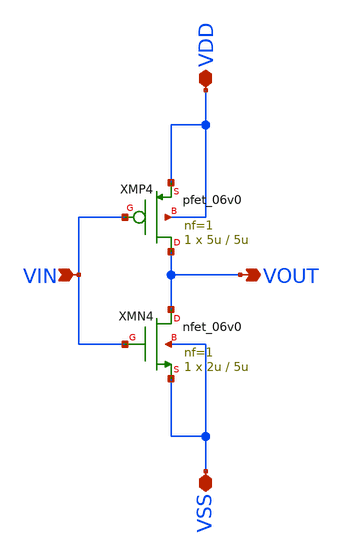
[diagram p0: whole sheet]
** sch_path: xschem/vco/vco_inv_forlvs.sch
**.subckt vco_inv_forlvs VIN VOUT VDD VSS
*.ipin VIN
*.opin VOUT
*.iopin VDD
*.iopin VSS
XMP4 VOUT VIN VDD VDD pfet_06v0 L=5u W=5u nf=1 ad='int((nf+1)/2) * W/nf * 0.18u' as='int((nf+2)/2) * W/nf * 0.18u'
+ pd='2*int((nf+1)/2) * (W/nf + 0.18u)' ps='2*int((nf+2)/2) * (W/nf + 0.18u)' nrd='0.18u / W' nrs='0.18u / W'
+ sa=0 sb=0 sd=0 m=1
XMN4 VOUT VIN VSS VSS nfet_06v0 L=5u W=2u nf=1 ad='int((nf+1)/2) * W/nf * 0.18u' as='int((nf+2)/2) * W/nf * 0.18u'
+ pd='2*int((nf+1)/2) * (W/nf + 0.18u)' ps='2*int((nf+2)/2) * (W/nf + 0.18u)' nrd='0.18u / W' nrs='0.18u / W'
+ sa=0 sb=0 sd=0 m=1
**.ends
.end
